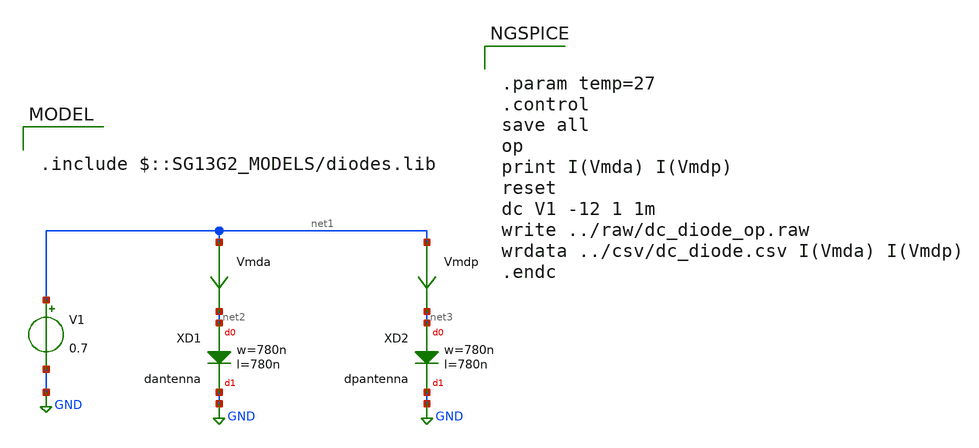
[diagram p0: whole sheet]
** sch_path: ihp-sg13g2/libs.tech/xschem/sg13g2_tests/dc_diode_op.sch
* Copyright 2023 IHP PDK Authors
**.subckt dc_diode_op
XXD1 net2 GND dantenna l=780n w=780n
XXD2 net3 GND dpantenna l=780n w=780n
V1 net1 GND 0.7
Vmda net1 net2 0
.save i(vmda)
Vmdp net1 net3 0
.save i(vmdp)
**** begin user architecture code

.include $::SG13G2_MODELS/diodes.lib



.param temp=27
.control
save all
op
print I(Vmda) I(Vmdp)
reset
dc V1 -12 1 1m
write ../raw/dc_diode_op.raw
wrdata ../csv/dc_diode.csv I(Vmda) I(Vmdp)
.endc


**** end user architecture code
**.ends
.GLOBAL GND
.end
